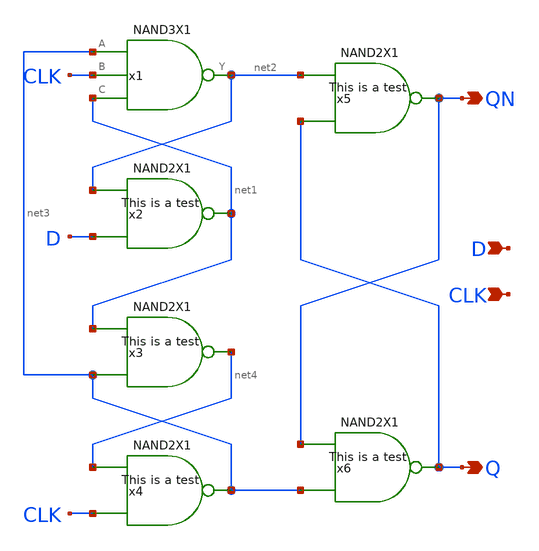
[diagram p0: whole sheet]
** sch_path: layout/xschem/sky130_rhbd/DFFX1.sch
**.subckt DFFX1 Q QN D CLK
*.opin Q
*.opin QN
*.ipin D
*.ipin CLK
x1 net2 net3 CLK net1 VDD VSS NAND3X1
x2 net1 net2 D VDD VSS NAND2X1
x3 net4 net1 net3 VDD VSS NAND2X1
x4 net3 net4 CLK VDD VSS NAND2X1
x5 QN net2 Q VDD VSS NAND2X1
x6 Q QN net3 VDD VSS NAND2X1
**.ends
.end
